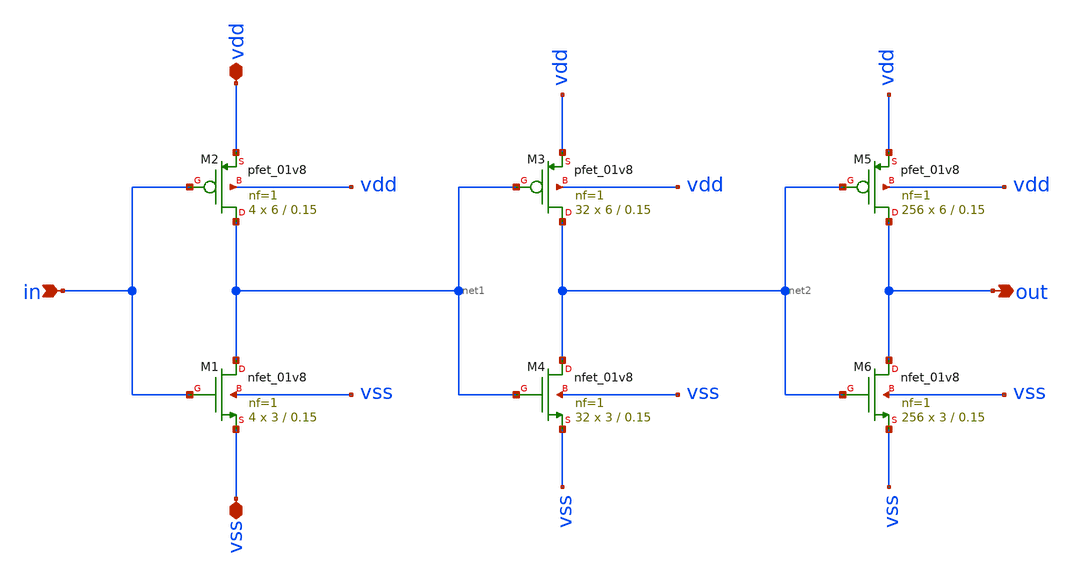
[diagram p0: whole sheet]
** sch_path: xschem/buffer_salida.sch
**.subckt buffer_salida vss in vdd out
*.iopin vss
*.ipin in
*.iopin vdd
*.opin out
XM2 net1 in vdd vdd sky130_fd_pr__pfet_01v8 L=0.15 W=6 nf=1 ad='int((nf+1)/2) * W/nf * 0.29' as='int((nf+2)/2) * W/nf * 0.29'
+ pd='2*int((nf+1)/2) * (W/nf + 0.29)' ps='2*int((nf+2)/2) * (W/nf + 0.29)' nrd='0.29 / W' nrs='0.29 / W'
+ sa=0 sb=0 sd=0 mult=4 m=4
XM1 net1 in vss vss sky130_fd_pr__nfet_01v8 L=0.15 W=3 nf=1 ad='int((nf+1)/2) * W/nf * 0.29' as='int((nf+2)/2) * W/nf * 0.29'
+ pd='2*int((nf+1)/2) * (W/nf + 0.29)' ps='2*int((nf+2)/2) * (W/nf + 0.29)' nrd='0.29 / W' nrs='0.29 / W'
+ sa=0 sb=0 sd=0 mult=4 m=4
XM3 net2 net1 vdd vdd sky130_fd_pr__pfet_01v8 L=0.15 W=6 nf=1 ad='int((nf+1)/2) * W/nf * 0.29' as='int((nf+2)/2) * W/nf * 0.29'
+ pd='2*int((nf+1)/2) * (W/nf + 0.29)' ps='2*int((nf+2)/2) * (W/nf + 0.29)' nrd='0.29 / W' nrs='0.29 / W'
+ sa=0 sb=0 sd=0 mult=32 m=32
XM4 net2 net1 vss vss sky130_fd_pr__nfet_01v8 L=0.15 W=3 nf=1 ad='int((nf+1)/2) * W/nf * 0.29' as='int((nf+2)/2) * W/nf * 0.29'
+ pd='2*int((nf+1)/2) * (W/nf + 0.29)' ps='2*int((nf+2)/2) * (W/nf + 0.29)' nrd='0.29 / W' nrs='0.29 / W'
+ sa=0 sb=0 sd=0 mult=32 m=32
XM5 out net2 vdd vdd sky130_fd_pr__pfet_01v8 L=0.15 W=6 nf=1 ad='int((nf+1)/2) * W/nf * 0.29' as='int((nf+2)/2) * W/nf * 0.29'
+ pd='2*int((nf+1)/2) * (W/nf + 0.29)' ps='2*int((nf+2)/2) * (W/nf + 0.29)' nrd='0.29 / W' nrs='0.29 / W'
+ sa=0 sb=0 sd=0 mult=256 m=256
XM6 out net2 vss vss sky130_fd_pr__nfet_01v8 L=0.15 W=3 nf=1 ad='int((nf+1)/2) * W/nf * 0.29' as='int((nf+2)/2) * W/nf * 0.29'
+ pd='2*int((nf+1)/2) * (W/nf + 0.29)' ps='2*int((nf+2)/2) * (W/nf + 0.29)' nrd='0.29 / W' nrs='0.29 / W'
+ sa=0 sb=0 sd=0 mult=256 m=256
**.ends
.end
